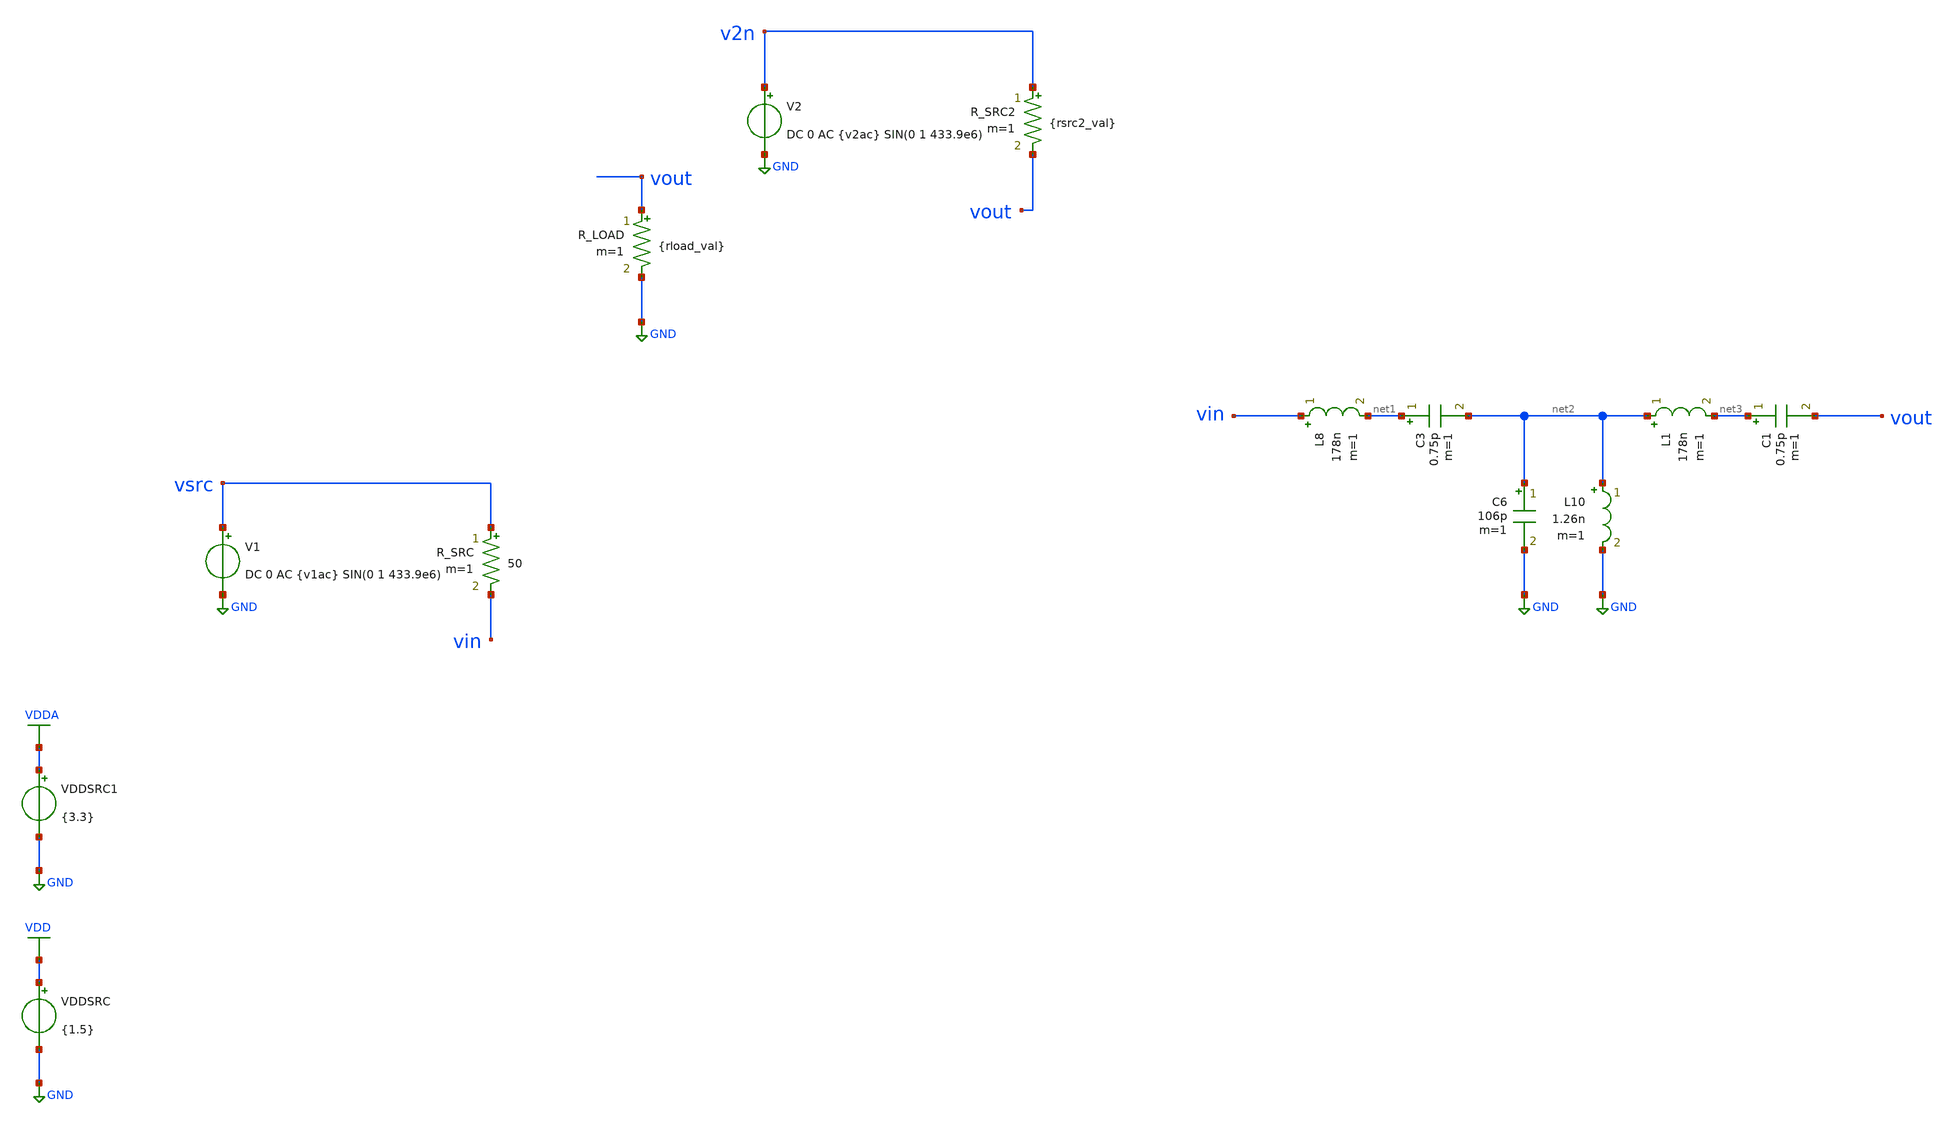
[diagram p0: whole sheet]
** sch_path: macros/heichips26_ook_top/testbenches/xschem/filter_tb_ac.sch
**.subckt filter_tb_ac
VDDSRC VDD GND {1.5}
VDDSRC1 VDDA GND {3.3}
V1 vsrc GND DC 0 AC {v1ac} SIN(0 1 433.9e6)
R_SRC vsrc vin 50 m=1
R_LOAD vout GND {rload_val} m=1
V2 v2n GND DC 0 AC {v2ac} SIN(0 1 433.9e6)
R_SRC2 v2n vout {rsrc2_val} m=1
C3 net1 net2 0.75p m=1
L8 vin net1 178n m=1
C6 net2 GND 106p m=1
L10 net2 GND 1.26n m=1
C1 net3 vout 0.75p m=1
L1 net2 net3 178n m=1
**** begin user architecture code


.param VDD=1.5
.param tr=1e-9
.param tr_data=50e-9
.param v1ac=1
.param v2ac=0
.param rload_val=50
.param rsrc2_val=50
.options klu reltol=1e-3 abstol=1e-12 vntol=1e-6 gmin=1e-12 itl1=200 itl4=100 rshunt=1e9 trtol=20
.save all
.control
alterparam v1ac=1
alterparam v2ac=0
alterparam rload_val=50
alterparam rsrc2_val=1e9
reset
ac lin 1001 100meg 1000meg
let Zin = v(vin)*50/(v(vsrc)-v(vin))
let S21_dB = db(2*v(vout)/v(vsrc))
let Zin_re = real(Zin)
let Zin_im = imag(Zin)
plot Zin_re Zin_im xlabel 'Frequency [Hz]' ylabel 'Zin [ohm]'
meas ac Zin_re_c find Zin_re when frequency=433.92e6
meas ac Zin_im_c find Zin_im when frequency=433.92e6
plot S21_dB xlabel 'Frequency [Hz]' ylabel 'S21 [dB]'
meas ac S21_center find S21_dB when frequency=433.92e6
echo
echo S21 at 433.92MHz = $&S21_center dB
echo Zin  at 433.92MHz = $&Zin_re_c + j$&Zin_im_c ohm

alterparam v1ac=0
alterparam v2ac=1
alterparam rload_val=1e9
alterparam rsrc2_val=50
reset
ac lin 1001 100meg 1000meg
let Zout = v(vout)*50/(v(v2n)-v(vout))
let Zout_re = real(Zout)
let Zout_im = imag(Zout)
plot Zout_re Zout_im xlabel 'Frequency [Hz]' ylabel 'Zout [ohm]'
meas ac Zout_re_c find Zout_re when frequency=433.92e6
meas ac Zout_im_c find Zout_im when frequency=433.92e6
echo
echo Zout at 433.92MHz = $&Zout_re_c + j$&Zout_im_c ohm
.endc



.lib cornerMOSlv.lib mos_tt
.lib cornerMOShv.lib mos_tt
.lib cornerRES.lib res_typ
.lib cornerDIO.lib dio_tt
.lib cornerCAP.lib cap_typ
.include /home/belal/HeiChips/heichips26-on-off/macros/heichips26_ook_top/macros/dac/netlist/xspice/dac.xspice
.include /home/belal/HeiChips/heichips26-on-off/macros/heichips26_ook_top/macros/ook_analog_system/netlist/pex/ook_transmitter_magic_pex_3.spice
.include /home/belal/HeiChips/heichips26-on-off/macros/heichips26_ook_top/macros/ook_analog_system/netlist/pex/ook_analog_system_magic_pex_3.spice
.include /home/belal/HeiChips/heichips26-on-off/IHP-Open-PDK/ihp-sg13cmos5l/libs.tech/ngspice/models/cap_mfringe.lib
.include /home/belal/HeiChips/heichips26-on-off/macros/heichips26_ook_top/macros/ook_analog_system/netlist/pex/vco_magic_pex_3.spice
.include /home/belal/HeiChips/heichips26-on-off/macros/heichips26_ook_top/macros/ook_analog_system/netlist/pex/output_buffer_magic_pex_3.spice
.include /home/belal/HeiChips/heichips26-on-off/macros/heichips26_ook_top/netlist/pex/heichips26_ook_top_magic_pex_3.spice
.include /home/belal/HeiChips/heichips26-on-off/IHP-Open-PDK/ihp-sg13cmos5l/libs.ref/sg13cmos5l_io/spice/sg13cmos5l_io.spi

**** end user architecture code
**.ends
.GLOBAL VDD
.GLOBAL GND
.GLOBAL VDDA
.end
